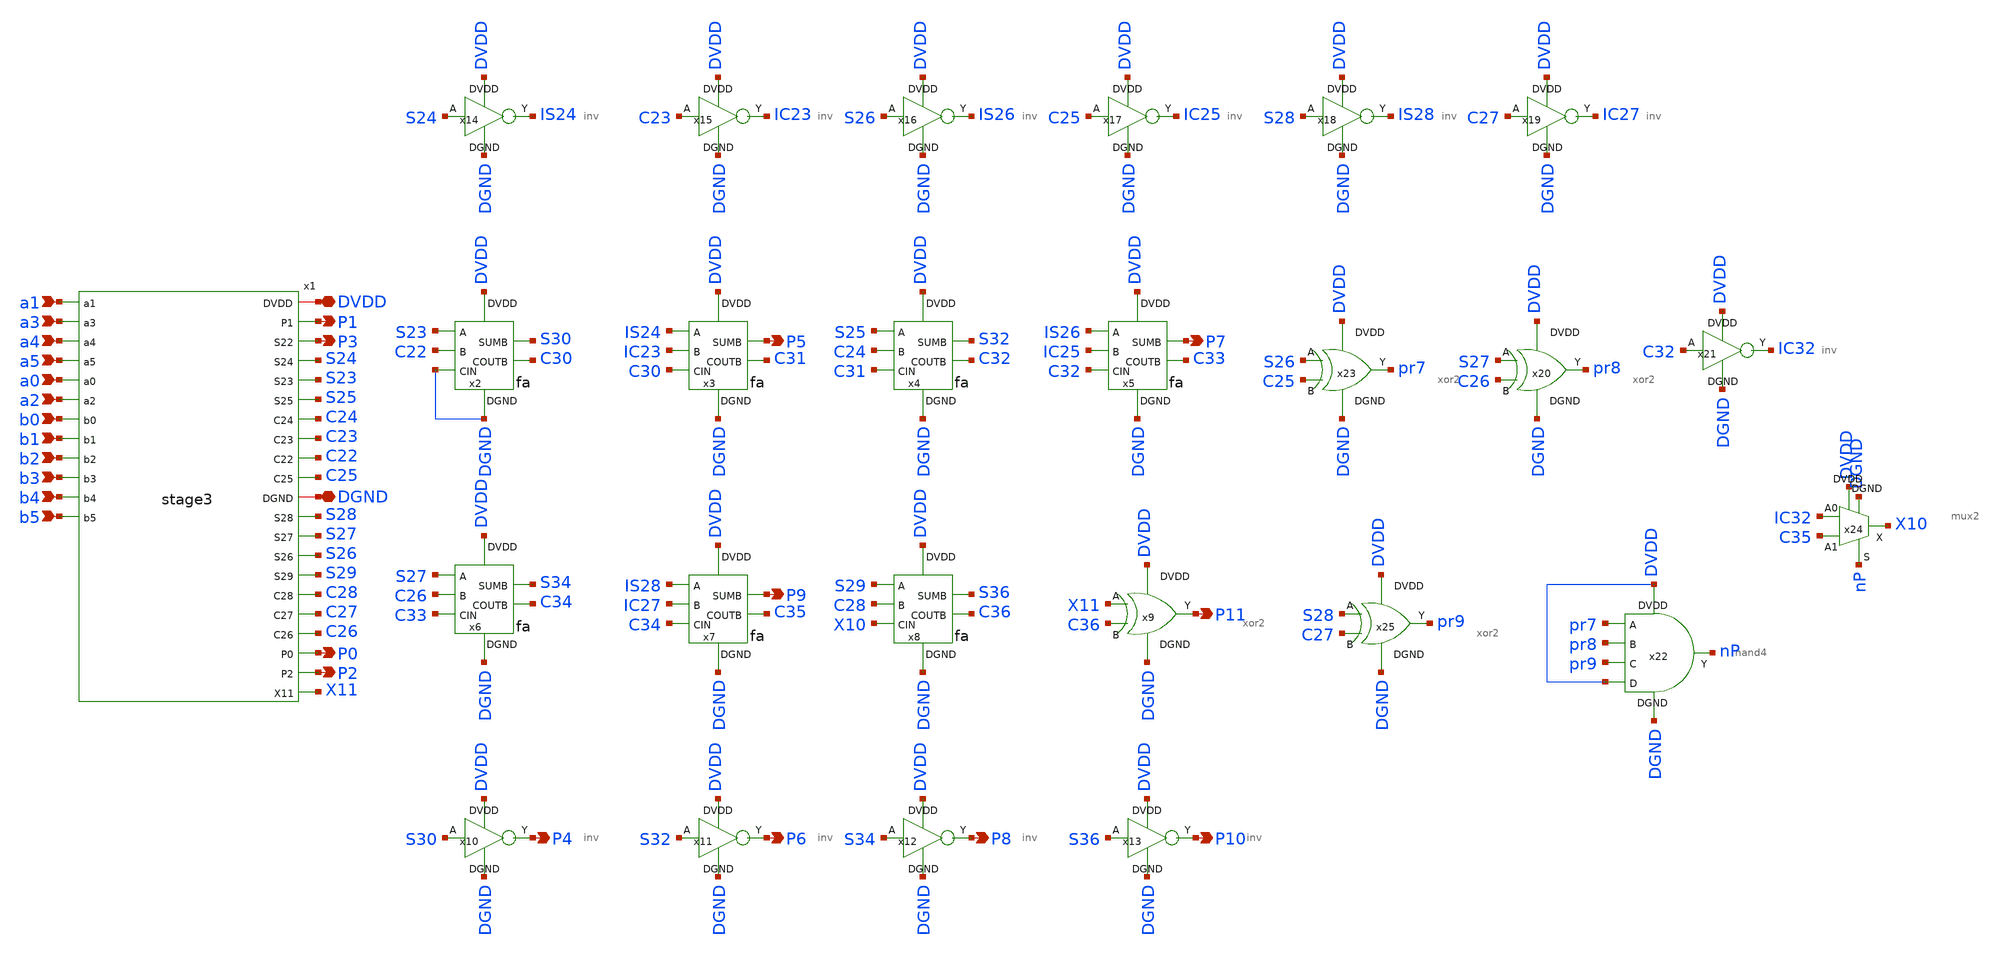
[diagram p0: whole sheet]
** sch_path: xschem/wallace.sch
**.subckt wallace a1 a3 a4 a5 a0 a2 b0 b1 b2 b3 b4 b5 DVDD DGND P1 P3 P0 P2 P11 P9 P7 P5 P4 P6 P8
*+ P10
*.ipin a1
*.ipin a3
*.ipin a4
*.ipin a5
*.ipin a0
*.ipin a2
*.ipin b0
*.ipin b1
*.ipin b2
*.ipin b3
*.ipin b4
*.ipin b5
*.iopin DVDD
*.iopin DGND
*.opin P1
*.opin P3
*.opin P0
*.opin P2
*.opin P11
*.opin P9
*.opin P7
*.opin P5
*.opin P4
*.opin P6
*.opin P8
*.opin P10
x2 DVDD DGND S23 C22 DGND C30 S30 fa
x3 DVDD DGND IS24 IC23 C30 C31 P5 fa
x4 DVDD DGND S25 C24 C31 C32 S32 fa
x5 DVDD DGND IS26 IC25 C32 C33 P7 fa
x6 DVDD DGND S27 C26 C33 C34 S34 fa
x7 DVDD DGND IS28 IC27 C34 C35 P9 fa
x8 DVDD DGND S29 C28 X10 C36 S36 fa
x9 DVDD X11 C36 P11 DGND xor2
x10 S30 P4 DVDD DGND inv
x11 S32 P6 DVDD DGND inv
x12 S34 P8 DVDD DGND inv
x13 S36 P10 DVDD DGND inv
x14 S24 IS24 DVDD DGND inv
x15 C23 IC23 DVDD DGND inv
x16 S26 IS26 DVDD DGND inv
x17 C25 IC25 DVDD DGND inv
x18 S28 IS28 DVDD DGND inv
x19 C27 IC27 DVDD DGND inv
x21 C32 IC32 DVDD DGND inv
x22 DVDD pr7 pr8 pr9 DVDD nP DGND nand4
x23 DVDD S26 C25 pr7 DGND xor2
x20 DVDD S27 C26 pr8 DGND xor2
x25 DVDD S28 C27 pr9 DGND xor2
x1 DVDD a1 a3 P1 a4 P3 S24 S23 S25 a5 C24 C23 C22 a0 C25 a2 b0 b1 b2 b3 DGND b4 b5 S28 S27 S26 S29
+ C28 C27 C26 P0 P2 X11 stage3
x24 DVDD nP IC32 C35 X10 DGND mux2
**.ends
.end
